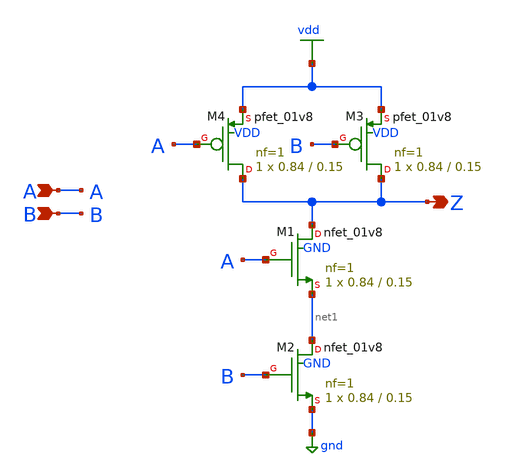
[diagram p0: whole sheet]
** sch_path: xschem/nand2.sch
**.subckt nand2 A B Z
*.ipin A
*.ipin B
*.opin Z
XM1 Z A net1 GND sky130_fd_pr__nfet_01v8 L=0.15 W=0.84 nf=1 ad='int((nf+1)/2) * W/nf * 0.29' as='int((nf+2)/2) * W/nf * 0.29'
+ pd='2*int((nf+1)/2) * (W/nf + 0.29)' ps='2*int((nf+2)/2) * (W/nf + 0.29)' nrd='0.29 / W' nrs='0.29 / W'
+ sa=0 sb=0 sd=0 mult=1 m=1
XM2 net1 B gnd GND sky130_fd_pr__nfet_01v8 L=0.15 W=0.84 nf=1 ad='int((nf+1)/2) * W/nf * 0.29' as='int((nf+2)/2) * W/nf * 0.29'
+ pd='2*int((nf+1)/2) * (W/nf + 0.29)' ps='2*int((nf+2)/2) * (W/nf + 0.29)' nrd='0.29 / W' nrs='0.29 / W'
+ sa=0 sb=0 sd=0 mult=1 m=1
XM3 Z B vdd VDD sky130_fd_pr__pfet_01v8 L=0.15 W=0.84 nf=1 ad='int((nf+1)/2) * W/nf * 0.29' as='int((nf+2)/2) * W/nf * 0.29'
+ pd='2*int((nf+1)/2) * (W/nf + 0.29)' ps='2*int((nf+2)/2) * (W/nf + 0.29)' nrd='0.29 / W' nrs='0.29 / W'
+ sa=0 sb=0 sd=0 mult=1 m=1
XM4 Z A vdd VDD sky130_fd_pr__pfet_01v8 L=0.15 W=0.84 nf=1 ad='int((nf+1)/2) * W/nf * 0.29' as='int((nf+2)/2) * W/nf * 0.29'
+ pd='2*int((nf+1)/2) * (W/nf + 0.29)' ps='2*int((nf+2)/2) * (W/nf + 0.29)' nrd='0.29 / W' nrs='0.29 / W'
+ sa=0 sb=0 sd=0 mult=1 m=1
**.ends
.GLOBAL gnd
.GLOBAL vdd
.end
